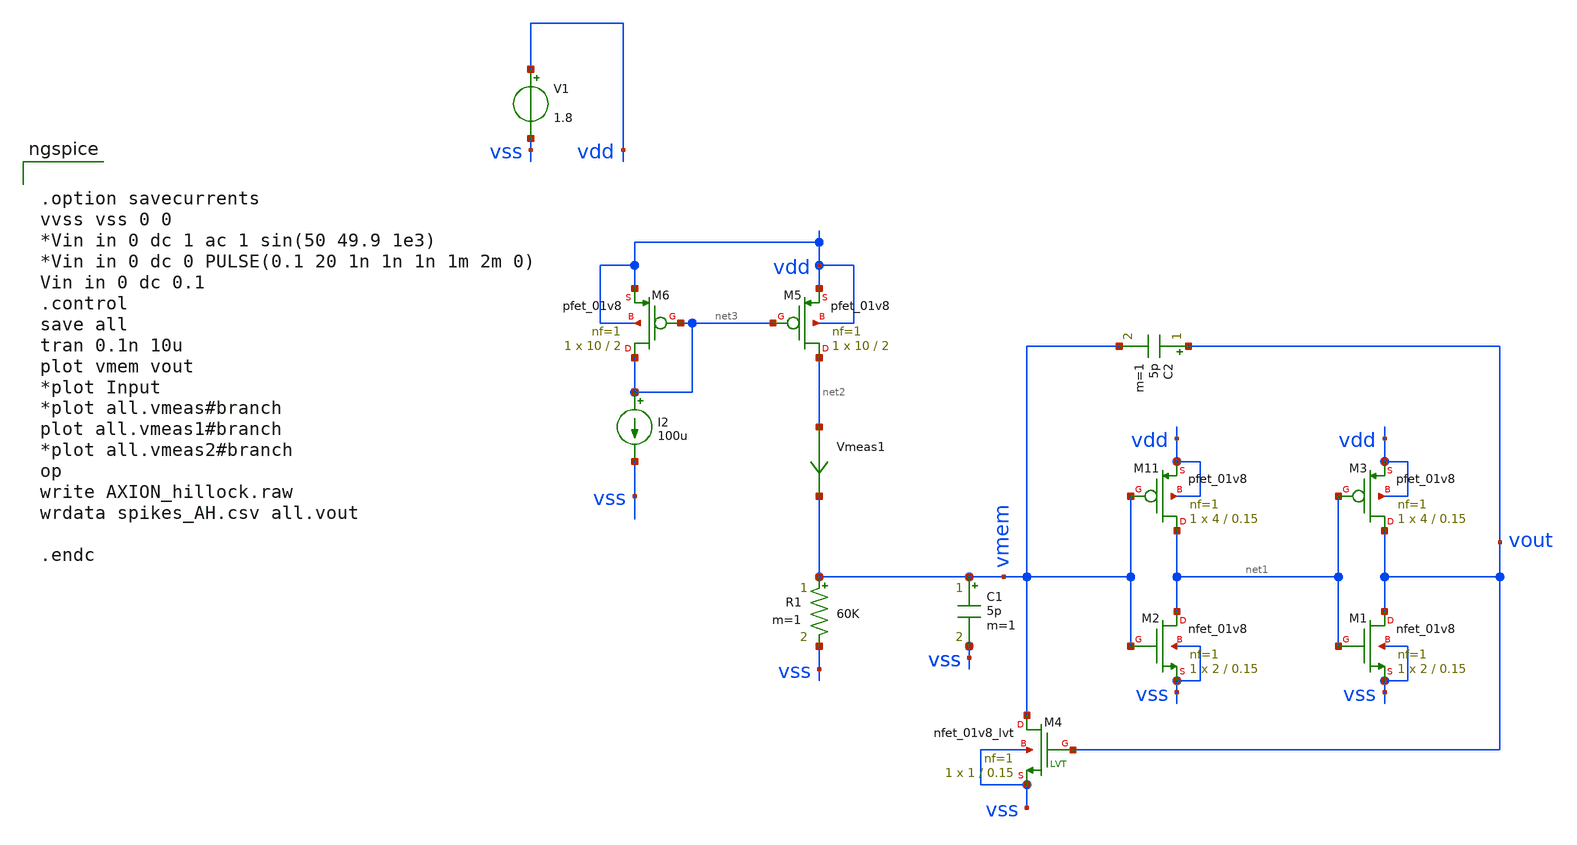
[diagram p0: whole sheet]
** sch_path: circuits/Axion_Hillock.sch
* Copyright 2020 Stefan Frederik Schippers
* Licensed under the Apache License, Version 2.0 (the "License");
* you may not use this file except in compliance with the License.
* You may obtain a copy of the License at
* https://www.apache.org/licenses/LICENSE-2.0
* Unless required by applicable law or agreed to in writing, software
* distributed under the License is distributed on an "AS IS" BASIS,
* WITHOUT WARRANTIES OR CONDITIONS OF ANY KIND, either express or implied.
* See the License for the specific language governing permissions and
* limitations under the License.
**.subckt Axion_Hillock
XM2 net1 vmem vss vss sky130_fd_pr__nfet_01v8 L=0.15 W=2 nf=1 ad='int((1 + 1)/2) * 2 / 1 * 0.29' as='int((1 + 2)/2) * 2 / 1 * 0.29'
+ pd='2*int((1 + 1)/2) * (2 / 1 + 0.29)' ps='2*int((1 + 2)/2) * (2 / 1 + 0.29)' nrd='0.29 / 2 ' nrs='0.29 / 2 '
+ sa=0 sb=0 sd=0 mult=1 m=1
XM11 net1 vmem vdd vdd sky130_fd_pr__pfet_01v8 L=0.15 W=4 nf=1 ad='int((nf+1)/2) * W/nf * 0.29' as='int((nf+2)/2) * W/nf * 0.29'
+ pd='2*int((nf+1)/2) * (W/nf + 0.29)' ps='2*int((nf+2)/2) * (W/nf + 0.29)' nrd='0.29 / W' nrs='0.29 / W'
+ sa=0 sb=0 sd=0 mult=1 m=1
XM1 vout net1 vss vss sky130_fd_pr__nfet_01v8 L=0.15 W=2 nf=1 ad='int((1 + 1)/2) * 2 / 1 * 0.29' as='int((1 + 2)/2) * 2 / 1 * 0.29'
+ pd='2*int((1 + 1)/2) * (2 / 1 + 0.29)' ps='2*int((1 + 2)/2) * (2 / 1 + 0.29)' nrd='0.29 / 2 ' nrs='0.29 / 2 '
+ sa=0 sb=0 sd=0 mult=1 m=1
XM3 vout net1 vdd vdd sky130_fd_pr__pfet_01v8 L=0.15 W=4 nf=1 ad='int((nf+1)/2) * W/nf * 0.29' as='int((nf+2)/2) * W/nf * 0.29'
+ pd='2*int((nf+1)/2) * (W/nf + 0.29)' ps='2*int((nf+2)/2) * (W/nf + 0.29)' nrd='0.29 / W' nrs='0.29 / W'
+ sa=0 sb=0 sd=0 mult=1 m=1
C2 vout vmem 5p m=1
V1 vdd vss 1.8
I2 net3 vss 100u
C1 vmem vss 5p m=1
Vmeas1 net2 vmem 0
.save i(vmeas1)
R1 vmem vss 60K m=1
XM5 net2 net3 vdd vdd sky130_fd_pr__pfet_01v8 L=2 W=10 nf=1 ad='int((nf+1)/2) * W/nf * 0.29' as='int((nf+2)/2) * W/nf * 0.29'
+ pd='2*int((nf+1)/2) * (W/nf + 0.29)' ps='2*int((nf+2)/2) * (W/nf + 0.29)' nrd='0.29 / W' nrs='0.29 / W'
+ sa=0 sb=0 sd=0 mult=1 m=1
XM6 net3 net3 vdd vdd sky130_fd_pr__pfet_01v8 L=2 W=10 nf=1 ad='int((nf+1)/2) * W/nf * 0.29' as='int((nf+2)/2) * W/nf * 0.29'
+ pd='2*int((nf+1)/2) * (W/nf + 0.29)' ps='2*int((nf+2)/2) * (W/nf + 0.29)' nrd='0.29 / W' nrs='0.29 / W'
+ sa=0 sb=0 sd=0 mult=1 m=1
XM4 vmem vout vss vss sky130_fd_pr__nfet_01v8_lvt L=0.15 W=1 nf=1 ad='int((1 + 1)/2) * 1 / 1 * 0.29'
+ as='int((1 + 2)/2) * 1 / 1 * 0.29' pd='2*int((1 + 1)/2) * (1 / 1 + 0.29)' ps='2*int((1 + 2)/2) * (1 / 1 + 0.29)'
+ nrd='0.29 / 1 ' nrs='0.29 / 1 ' sa=0 sb=0 sd=0 mult=1 m=1
**** begin user architecture code


.option savecurrents
vvss vss 0 0
*Vin in 0 dc 1 ac 1 sin(50 49.9 1e3)
*Vin in 0 dc 0 PULSE(0.1 20 1n 1n 1n 1m 2m 0)
Vin in 0 dc 0.1
.control
save all
tran 0.1n 10u
plot vmem vout
*plot Input
*plot all.vmeas#branch
plot all.vmeas1#branch
*plot all.vmeas2#branch
op
write AXION_hillock.raw
wrdata spikes_AH.csv all.vout

.endc


 .lib $::SKYWATER_MODELS/models/sky130.lib.spice tt

.param mc_mm_switch=0
.param mc_pr_switch=1


**** end user architecture code
**.ends
.end
